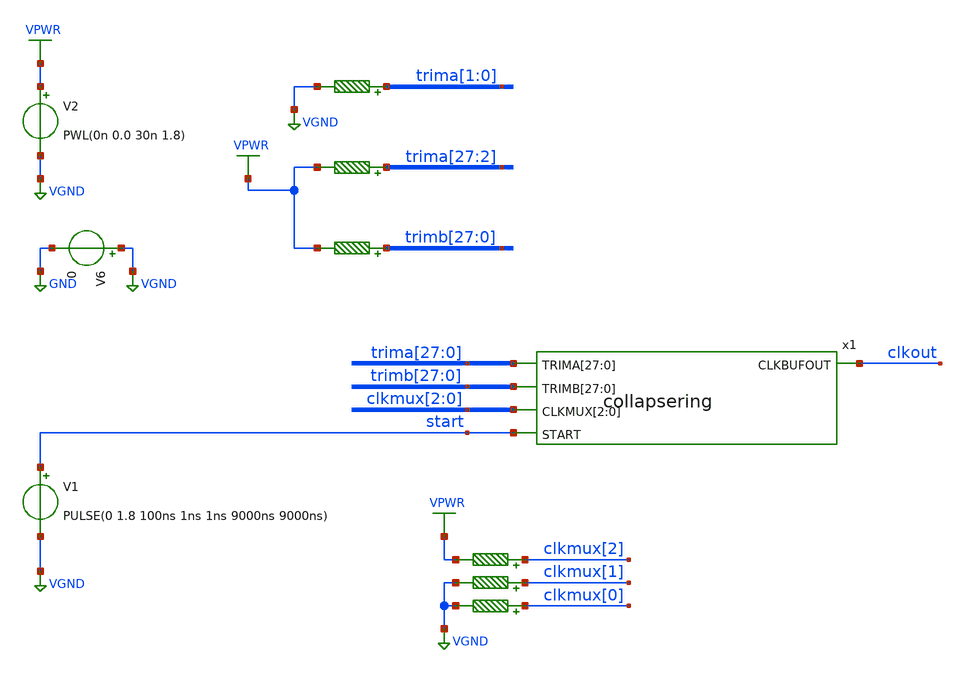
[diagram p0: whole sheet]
** sch_path: ip/randsack/sch/collapsering_tb.sch
**.subckt collapsering_tb
V1 start VGND PULSE(0 1.8 100ns 1ns 1ns 9000ns 9000ns)
V2 VPWR VGND PWL(0n 0.0 30n 1.8)
V6 VGND GND 0
R1[1] trima[1] VGND 0.01 m=1
R1[0] trima[0] VGND 0.01 m=1
R2[27] trima[27] VPWR 0.01 m=1
R2[26] trima[26] VPWR 0.01 m=1
R2[25] trima[25] VPWR 0.01 m=1
R2[24] trima[24] VPWR 0.01 m=1
R2[23] trima[23] VPWR 0.01 m=1
R2[22] trima[22] VPWR 0.01 m=1
R2[21] trima[21] VPWR 0.01 m=1
R2[20] trima[20] VPWR 0.01 m=1
R2[19] trima[19] VPWR 0.01 m=1
R2[18] trima[18] VPWR 0.01 m=1
R2[17] trima[17] VPWR 0.01 m=1
R2[16] trima[16] VPWR 0.01 m=1
R2[15] trima[15] VPWR 0.01 m=1
R2[14] trima[14] VPWR 0.01 m=1
R2[13] trima[13] VPWR 0.01 m=1
R2[12] trima[12] VPWR 0.01 m=1
R2[11] trima[11] VPWR 0.01 m=1
R2[10] trima[10] VPWR 0.01 m=1
R2[9] trima[9] VPWR 0.01 m=1
R2[8] trima[8] VPWR 0.01 m=1
R2[7] trima[7] VPWR 0.01 m=1
R2[6] trima[6] VPWR 0.01 m=1
R2[5] trima[5] VPWR 0.01 m=1
R2[4] trima[4] VPWR 0.01 m=1
R2[3] trima[3] VPWR 0.01 m=1
R2[2] trima[2] VPWR 0.01 m=1
R3[27] trimb[27] VPWR 0.01 m=1
R3[26] trimb[26] VPWR 0.01 m=1
R3[25] trimb[25] VPWR 0.01 m=1
R3[24] trimb[24] VPWR 0.01 m=1
R3[23] trimb[23] VPWR 0.01 m=1
R3[22] trimb[22] VPWR 0.01 m=1
R3[21] trimb[21] VPWR 0.01 m=1
R3[20] trimb[20] VPWR 0.01 m=1
R3[19] trimb[19] VPWR 0.01 m=1
R3[18] trimb[18] VPWR 0.01 m=1
R3[17] trimb[17] VPWR 0.01 m=1
R3[16] trimb[16] VPWR 0.01 m=1
R3[15] trimb[15] VPWR 0.01 m=1
R3[14] trimb[14] VPWR 0.01 m=1
R3[13] trimb[13] VPWR 0.01 m=1
R3[12] trimb[12] VPWR 0.01 m=1
R3[11] trimb[11] VPWR 0.01 m=1
R3[10] trimb[10] VPWR 0.01 m=1
R3[9] trimb[9] VPWR 0.01 m=1
R3[8] trimb[8] VPWR 0.01 m=1
R3[7] trimb[7] VPWR 0.01 m=1
R3[6] trimb[6] VPWR 0.01 m=1
R3[5] trimb[5] VPWR 0.01 m=1
R3[4] trimb[4] VPWR 0.01 m=1
R3[3] trimb[3] VPWR 0.01 m=1
R3[2] trimb[2] VPWR 0.01 m=1
R3[1] trimb[1] VPWR 0.01 m=1
R3[0] trimb[0] VPWR 0.01 m=1
x1 trima[27] trima[26] trima[25] trima[24] trima[23] trima[22] trima[21] trima[20] trima[19]
+ trima[18] trima[17] trima[16] trima[15] trima[14] trima[13] trima[12] trima[11] trima[10] trima[9] trima[8]
+ trima[7] trima[6] trima[5] trima[4] trima[3] trima[2] trima[1] trima[0] trimb[27] trimb[26] trimb[25]
+ trimb[24] trimb[23] trimb[22] trimb[21] trimb[20] trimb[19] trimb[18] trimb[17] trimb[16] trimb[15] trimb[14]
+ trimb[13] trimb[12] trimb[11] trimb[10] trimb[9] trimb[8] trimb[7] trimb[6] trimb[5] trimb[4] trimb[3]
+ trimb[2] trimb[1] trimb[0] clkmux[2] clkmux[1] clkmux[0] start clkout collapsering
R1 clkmux[2] VPWR 0.01 m=1
R2 clkmux[1] VGND 0.01 m=1
R3 clkmux[0] VGND 0.01 m=1
**** begin user architecture code


.lib /home/harrison/workspace/sky130/sky130A/libs.tech/ngspice/sky130.lib.spice tt
.include /home/harrison/workspace/sky130/sky130A/libs.ref/sky130_fd_sc_hd/spice/sky130_fd_sc_hd.spice

.option TEMP=27
* .option RELTOL=1.0E-1

.control
save all
tran 0.1n 10u
write collapsering_tb.out
.endc


**** end user architecture code
**.ends

* expanding   symbol:  /home/harrison/workspace/randsack/ip/randsack/sch/collapsering.sym # of
*+ pins=5
** sym_path: ip/randsack/sch/collapsering.sym
** sch_path: ip/randsack/sch/collapsering.sch
.subckt collapsering TRIMA[27] TRIMA[26] TRIMA[25] TRIMA[24] TRIMA[23] TRIMA[22] TRIMA[21] TRIMA[20]
+ TRIMA[19] TRIMA[18] TRIMA[17] TRIMA[16] TRIMA[15] TRIMA[14] TRIMA[13] TRIMA[12] TRIMA[11] TRIMA[10] TRIMA[9]
+ TRIMA[8] TRIMA[7] TRIMA[6] TRIMA[5] TRIMA[4] TRIMA[3] TRIMA[2] TRIMA[1] TRIMA[0] TRIMB[27] TRIMB[26]
+ TRIMB[25] TRIMB[24] TRIMB[23] TRIMB[22] TRIMB[21] TRIMB[20] TRIMB[19] TRIMB[18] TRIMB[17] TRIMB[16] TRIMB[15]
+ TRIMB[14] TRIMB[13] TRIMB[12] TRIMB[11] TRIMB[10] TRIMB[9] TRIMB[8] TRIMB[7] TRIMB[6] TRIMB[5] TRIMB[4]
+ TRIMB[3] TRIMB[2] TRIMB[1] TRIMB[0] CLKMUX[2] CLKMUX[1] CLKMUX[0] START CLKBUFOUT
*.opin CLKBUFOUT
*.ipin START
*.ipin
*+ TRIMA[27],TRIMA[26],TRIMA[25],TRIMA[24],TRIMA[23],TRIMA[22],TRIMA[21],TRIMA[20],TRIMA[19],TRIMA[18],TRIMA[17],TRIMA[16],TRIMA[15],TRIMA[14],TRIMA[13],TRIMA[12],TRIMA[11],TRIMA[10],TRIMA[9],TRIMA[8],TRIMA[7],TRIMA[6],TRIMA[5],TRIMA[4],TRIMA[3],TRIMA[2],TRIMA[1],TRIMA[0]
*.ipin
*+ TRIMB[27],TRIMB[26],TRIMB[25],TRIMB[24],TRIMB[23],TRIMB[22],TRIMB[21],TRIMB[20],TRIMB[19],TRIMB[18],TRIMB[17],TRIMB[16],TRIMB[15],TRIMB[14],TRIMB[13],TRIMB[12],TRIMB[11],TRIMB[10],TRIMB[9],TRIMB[8],TRIMB[7],TRIMB[6],TRIMB[5],TRIMB[4],TRIMB[3],TRIMB[2],TRIMB[1],TRIMB[0]
*.ipin CLKMUX[2],CLKMUX[1],CLKMUX[0]
x21 outb net25 VGND VNB VPB VPWR net1 sky130_fd_sc_hd__nand2_4
x47 net25 outa VGND VNB VPB VPWR net16 sky130_fd_sc_hd__nand2_4
x35 net38 VGND VNB VPB VPWR CLKBUFOUT sky130_fd_sc_hd__clkbuf_4
x1 net2 net1 TRIMA[0] TRIMA[1] triminv
x2 net3 net2 TRIMA[2] TRIMA[3] triminv
x3 net4 net3 TRIMA[4] TRIMA[5] triminv
x4 net5 net4 TRIMA[6] TRIMA[7] triminv
x5 net6 net5 TRIMA[8] TRIMA[9] triminv
x6 net7 net6 TRIMA[10] TRIMA[11] triminv
x7 net8 net7 TRIMA[12] TRIMA[13] triminv
x8 net24 net8 TRIMA[14] TRIMA[15] triminv
x9 net17 net24 TRIMA[16] TRIMA[17] triminv
x10 net18 net17 TRIMA[18] TRIMA[19] triminv
x11 net19 net18 TRIMA[20] TRIMA[21] triminv
x12 net39 net19 TRIMA[22] TRIMA[23] triminv
x13 net9 net16 TRIMB[0] TRIMB[1] triminv
x14 net10 net9 TRIMB[2] TRIMB[3] triminv
x15 net11 net10 TRIMB[4] TRIMB[5] triminv
x16 net12 net11 TRIMB[6] TRIMB[7] triminv
x17 net13 net12 TRIMB[8] TRIMB[9] triminv
x18 net14 net13 TRIMB[10] TRIMB[11] triminv
x19 net15 net14 TRIMB[12] TRIMB[13] triminv
x20 net23 net15 TRIMB[14] TRIMB[15] triminv
x22 net20 net23 TRIMB[16] TRIMB[17] triminv
x23 net21 net20 TRIMB[18] TRIMB[19] triminv
x24 net22 net21 TRIMB[20] TRIMB[21] triminv
x25 net41 net22 TRIMB[22] TRIMB[23] triminv
x27 clk_ff0 net27 VGND VNB VPB VPWR clk_ff1 net27 sky130_fd_sc_hd__dfxbp_2
x28 clk_ff0 net28 VGND VNB VPB VPWR net26 net28 sky130_fd_sc_hd__dfxbp_2
x29 net26 net29 VGND VNB VPB VPWR clk_ff2 net29 sky130_fd_sc_hd__dfxbp_2
x26 net30 VGND VNB VPB VPWR clk_ff0 sky130_fd_sc_hd__clkbuf_8
x30 clk_ff0 clk_ff1 clk_ff2 clk_ff3 CLKMUX[0] CLKMUX[1] VGND VNB VPB VPWR net38
+ sky130_fd_sc_hd__mux4_2
x31 clk_ff0 net32 VGND VNB VPB VPWR net31 net32 sky130_fd_sc_hd__dfxbp_2
x32 net31 net33 VGND VNB VPB VPWR net34 net33 sky130_fd_sc_hd__dfxbp_2
x33 net34 net35 VGND VNB VPB VPWR clk_ff3 net35 sky130_fd_sc_hd__dfxbp_2
x34 net36 net37 CLKMUX[2] VGND VNB VPB VPWR net30 sky130_fd_sc_hd__mux2_2
x36 outb VGND VNB VPB VPWR net36 sky130_fd_sc_hd__clkbuf_2
x37 outa VGND VNB VPB VPWR net37 sky130_fd_sc_hd__clkbuf_2
x38 START VGND VNB VPB VPWR net25 sky130_fd_sc_hd__clkbuf_2
x39 net40 net39 TRIMA[24] TRIMA[25] triminv
x40 outa net40 TRIMA[26] TRIMA[27] triminv
x41 net42 net41 TRIMB[24] TRIMB[25] triminv
x42 outb net42 TRIMB[26] TRIMB[27] triminv
.ends


* expanding   symbol:  /home/harrison/workspace/randsack/ip/randsack/sch/triminv.sym # of pins=4
** sym_path: ip/randsack/sch/triminv.sym
** sch_path: ip/randsack/sch/triminv.sch
.subckt triminv OUT IN TRIM0 TRIM1
*.ipin IN
*.ipin OUT
*.ipin TRIM0
*.ipin TRIM1
x1 IN VGND VNB VPB VPWR ts sky130_fd_sc_hd__clkbuf_2
x2 ts TRIM1 VGND VNB VPB VPWR d1 sky130_fd_sc_hd__einvn_4
x3 d1 VGND VNB VPB VPWR d2 sky130_fd_sc_hd__clkinv_1
x4 d2 TRIM0 VGND VNB VPB VPWR OUT sky130_fd_sc_hd__einvp_2
x5 ts VGND VNB VPB VPWR d0 sky130_fd_sc_hd__clkbuf_1
x6 d0 TRIM1 VGND VNB VPB VPWR d1 sky130_fd_sc_hd__einvp_2
x7 ts TRIM0 VGND VNB VPB VPWR OUT sky130_fd_sc_hd__einvn_8
.ends

.GLOBAL VPWR
.GLOBAL VGND
.GLOBAL GND
.end
